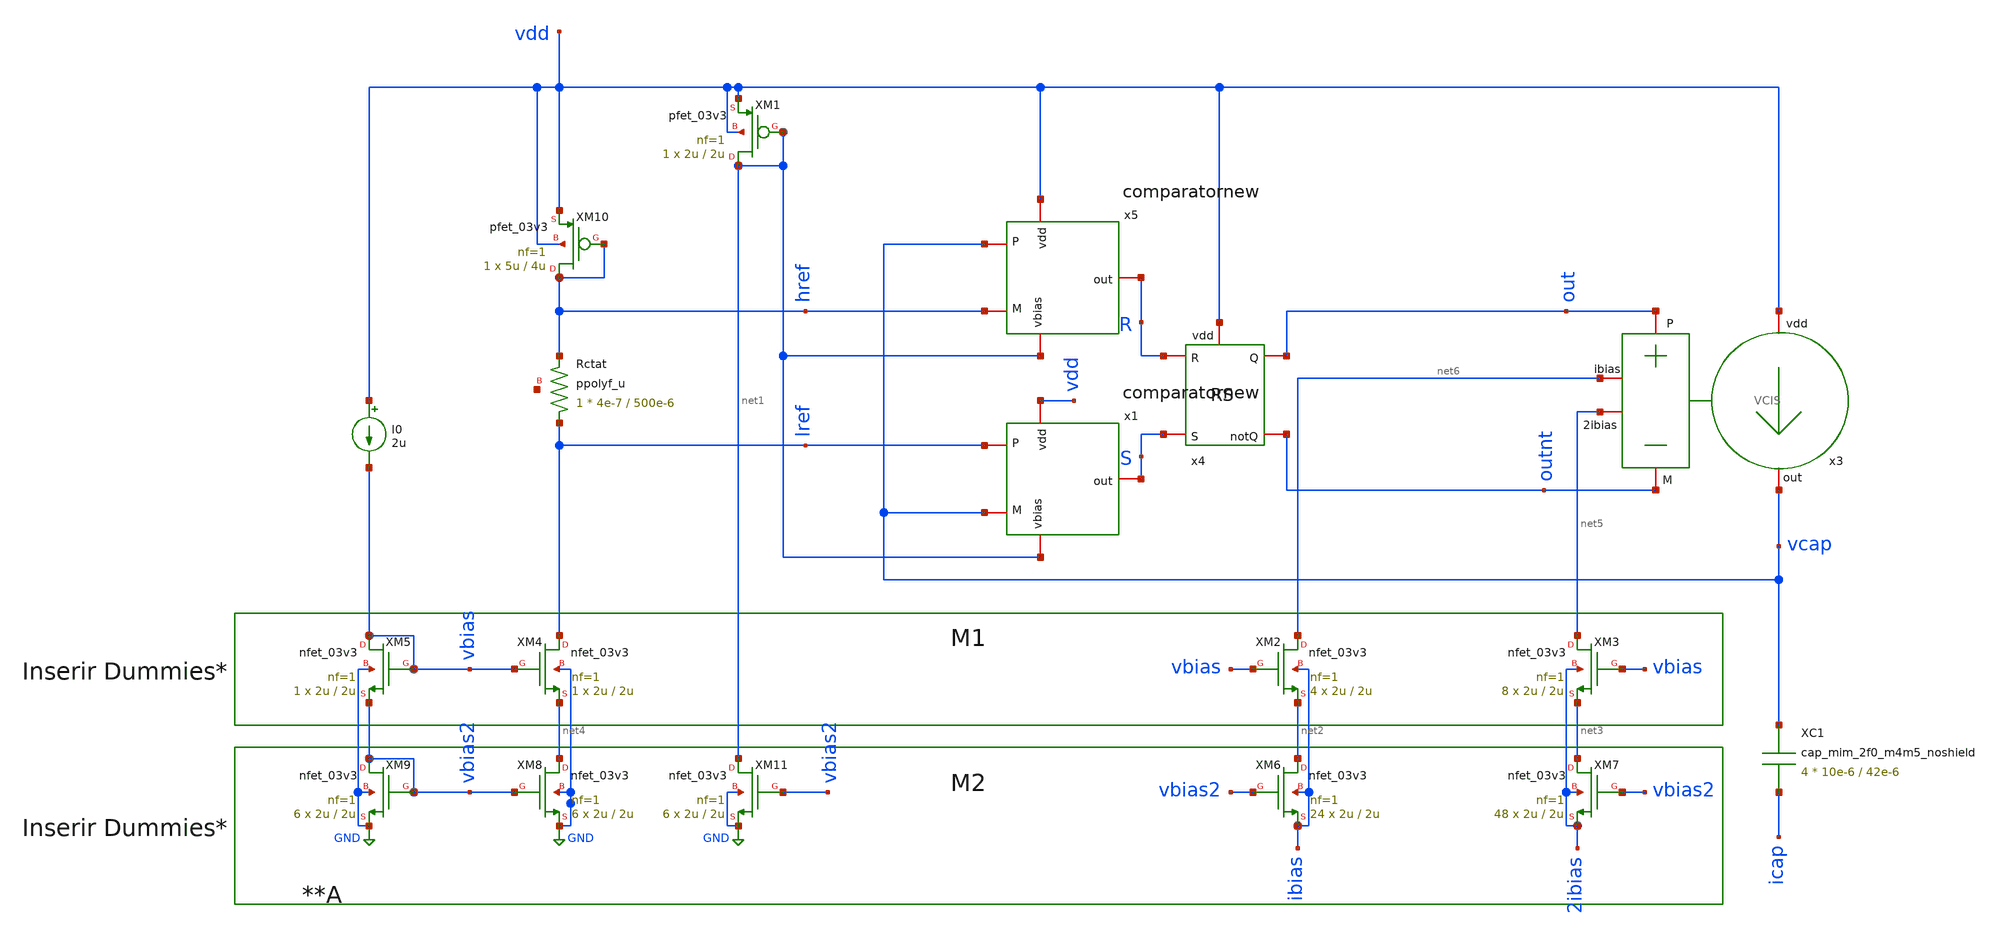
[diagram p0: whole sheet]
** sch_path: Clock_Reference/untitled.sch
**.subckt untitled
XM1 net1 net1 vdd vdd pfet_03v3 L=2u W=2u nf=1 ad='int((nf+1)/2) * W/nf * 0.18u' as='int((nf+2)/2) * W/nf * 0.18u'
+ pd='2*int((nf+1)/2) * (W/nf + 0.18u)' ps='2*int((nf+2)/2) * (W/nf + 0.18u)' nrd='0.18u / W' nrs='0.18u / W'
+ sa=0 sb=0 sd=0 m=1
XM2 net6 vbias net2 ibias nfet_03v3 L=2u W=2u nf=1 ad='int((nf+1)/2) * W/nf * 0.18u' as='int((nf+2)/2) * W/nf * 0.18u'
+ pd='2*int((nf+1)/2) * (W/nf + 0.18u)' ps='2*int((nf+2)/2) * (W/nf + 0.18u)' nrd='0.18u / W' nrs='0.18u / W'
+ sa=0 sb=0 sd=0 m=4
XM3 net5 vbias net3 2ibias nfet_03v3 L=2u W=2u nf=1 ad='int((nf+1)/2) * W/nf * 0.18u' as='int((nf+2)/2) * W/nf * 0.18u'
+ pd='2*int((nf+1)/2) * (W/nf + 0.18u)' ps='2*int((nf+2)/2) * (W/nf + 0.18u)' nrd='0.18u / W' nrs='0.18u / W'
+ sa=0 sb=0 sd=0 m=8
XM4 lref vbias net4 GND nfet_03v3 L=2u W=2u nf=1 ad='int((nf+1)/2) * W/nf * 0.18u' as='int((nf+2)/2) * W/nf * 0.18u'
+ pd='2*int((nf+1)/2) * (W/nf + 0.18u)' ps='2*int((nf+2)/2) * (W/nf + 0.18u)' nrd='0.18u / W' nrs='0.18u / W'
+ sa=0 sb=0 sd=0 m=1
XM5 vbias vbias vbias2 GND nfet_03v3 L=2u W=2u nf=1 ad='int((nf+1)/2) * W/nf * 0.18u' as='int((nf+2)/2) * W/nf * 0.18u'
+ pd='2*int((nf+1)/2) * (W/nf + 0.18u)' ps='2*int((nf+2)/2) * (W/nf + 0.18u)' nrd='0.18u / W' nrs='0.18u / W'
+ sa=0 sb=0 sd=0 m=1
I0 vdd vbias 2u
XM6 net2 vbias2 ibias ibias nfet_03v3 L=2u W=2u nf=1 ad='int((nf+1)/2) * W/nf * 0.18u' as='int((nf+2)/2) * W/nf * 0.18u'
+ pd='2*int((nf+1)/2) * (W/nf + 0.18u)' ps='2*int((nf+2)/2) * (W/nf + 0.18u)' nrd='0.18u / W' nrs='0.18u / W'
+ sa=0 sb=0 sd=0 m=24
XM7 net3 vbias2 2ibias 2ibias nfet_03v3 L=2u W=2u nf=1 ad='int((nf+1)/2) * W/nf * 0.18u' as='int((nf+2)/2) * W/nf * 0.18u'
+ pd='2*int((nf+1)/2) * (W/nf + 0.18u)' ps='2*int((nf+2)/2) * (W/nf + 0.18u)' nrd='0.18u / W' nrs='0.18u / W'
+ sa=0 sb=0 sd=0 m=48
XM8 net4 vbias2 GND GND nfet_03v3 L=2u W=2u nf=1 ad='int((nf+1)/2) * W/nf * 0.18u' as='int((nf+2)/2) * W/nf * 0.18u'
+ pd='2*int((nf+1)/2) * (W/nf + 0.18u)' ps='2*int((nf+2)/2) * (W/nf + 0.18u)' nrd='0.18u / W' nrs='0.18u / W'
+ sa=0 sb=0 sd=0 m=6
XM9 vbias2 vbias2 GND GND nfet_03v3 L=2u W=2u nf=1 ad='int((nf+1)/2) * W/nf * 0.18u' as='int((nf+2)/2) * W/nf * 0.18u'
+ pd='2*int((nf+1)/2) * (W/nf + 0.18u)' ps='2*int((nf+2)/2) * (W/nf + 0.18u)' nrd='0.18u / W' nrs='0.18u / W'
+ sa=0 sb=0 sd=0 m=6
XRctat lref href net7 ppolyf_u r_width=4e-7 r_length=500e-6 m=1
XM10 href href vdd vdd pfet_03v3 L=4u W=5u nf=1 ad='int((nf+1)/2) * W/nf * 0.18u' as='int((nf+2)/2) * W/nf * 0.18u'
+ pd='2*int((nf+1)/2) * (W/nf + 0.18u)' ps='2*int((nf+2)/2) * (W/nf + 0.18u)' nrd='0.18u / W' nrs='0.18u / W'
+ sa=0 sb=0 sd=0 m=1
XM11 net1 vbias2 GND GND nfet_03v3 L=2u W=2u nf=1 ad='int((nf+1)/2) * W/nf * 0.18u' as='int((nf+2)/2) * W/nf * 0.18u'
+ pd='2*int((nf+1)/2) * (W/nf + 0.18u)' ps='2*int((nf+2)/2) * (W/nf + 0.18u)' nrd='0.18u / W' nrs='0.18u / W'
+ sa=0 sb=0 sd=0 m=6
x3 vdd vcap out outnt net6 net5 VCIS
x4 vdd R S out outnt RS
x5 vdd net1 vcap href R comparatornew
x1 vdd net1 lref vcap S comparatornew
XC1 vcap icap cap_mim_2f0_m4m5_noshield c_width=10e-6 c_length=42e-6 m=4
**** begin user architecture code

.include /home/gmaranhao/Desktop/Bracolin/padframe/openfasoc-io-tb/gf180mcu_fd_io.spice
XDUT0 VDD CS DVDD DVSS IE OE PAD0 VDD VSS VSS VSS SL VDD VSS Y0 gf180mcu_fd_io__bi_t
XDUT1 VSS CS DVDD DVSS IE OE PAD1 VSS VSS VSS VDD SL VDD VSS Y1 gf180mcu_fd_io__bi_t



vvdd vdd 0 3.3
vcurr curr 0 0
vibias ibias 0 0
v2ibias 2ibias 0 0
vicap icap 0 0

.control
save all

let temperature = -40

while temperature<130
 reset
 set temp = $&temperature
 remzerovec
 tran 1n 5000n
 write clockGenerator.raw
 set appendwrite

 *wrdata /home/cesaralbuquerque/Desktop/out/transient[$&temperature].txt V(out)
 let temperature = temperature + 20
end
.endc
.save all



.include $::180MCU_MODELS/design.ngspice
.lib $::180MCU_MODELS/sm141064.ngspice typical
.lib $::180MCU_MODELS/sm141064.ngspice res_typical
.lib $::180MCU_MODELS/sm141064.ngspice moscap_typical
.lib $::180MCU_MODELS/sm141064.ngspice mimcap_typical
.lib $::180MCU_MODELS/sm141064.ngspice cap_mim
*.lib $::180MCU_MODELS/sm141064.ngspice res_statistical
*.param sw_stat_mismatch=1
*.param sw_stat_global=1

**** end user architecture code
**.ends
.GLOBAL GND
.end
